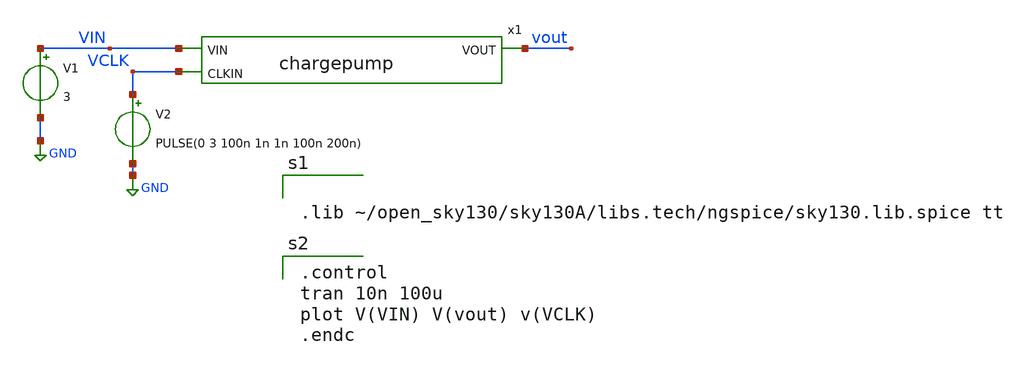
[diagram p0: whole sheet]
** sch_path: xschem/charge_pump/chargepump_tb.sch
**.subckt chargepump_tb
x1 VIN vout VCLK chargepump
V1 VIN GND 3
V2 VCLK GND PULSE(0 3 100n 1n 1n 100n 200n)
**** begin user architecture code


.lib ~/open_sky130/sky130A/libs.tech/ngspice/sky130.lib.spice tt


.control
tran 10n 100u
plot V(VIN) V(vout) v(VCLK)
.endc

**** end user architecture code
**.ends

* expanding   symbol:  chargepump.sym # of pins=3
** sym_path: xschem/charge_pump/chargepump.sym
** sch_path: xschem/charge_pump/chargepump.sch
.subckt chargepump VIN VOUT CLKIN
*.ipin VIN
*.ipin CLKIN
*.opin VOUT
XM2 VOUT net1 net1 net1 sky130_fd_pr__nfet_03v3_nvt L=0.5 W=1 nf=1 ad='int((nf+1)/2) * W/nf * 0.29' as='int((nf+2)/2) * W/nf * 0.29'
+ pd='2*int((nf+1)/2) * (W/nf + 0.29)' ps='2*int((nf+2)/2) * (W/nf + 0.29)' nrd='0.29 / W' nrs='0.29 / W'
+ sa=0 sb=0 sd=0 mult=1 m=1
XM1 VOUT net1 net1 net1 sky130_fd_pr__nfet_03v3_nvt L=0.5 W=1 nf=1 ad='int((nf+1)/2) * W/nf * 0.29' as='int((nf+2)/2) * W/nf * 0.29'
+ pd='2*int((nf+1)/2) * (W/nf + 0.29)' ps='2*int((nf+2)/2) * (W/nf + 0.29)' nrd='0.29 / W' nrs='0.29 / W'
+ sa=0 sb=0 sd=0 mult=1 m=1
XM3 net1 VIN VIN VIN sky130_fd_pr__nfet_03v3_nvt L=0.5 W=1 nf=1 ad='int((nf+1)/2) * W/nf * 0.29' as='int((nf+2)/2) * W/nf * 0.29'
+ pd='2*int((nf+1)/2) * (W/nf + 0.29)' ps='2*int((nf+2)/2) * (W/nf + 0.29)' nrd='0.29 / W' nrs='0.29 / W'
+ sa=0 sb=0 sd=0 mult=1 m=1
XM4 net1 VIN VIN VIN sky130_fd_pr__nfet_03v3_nvt L=0.5 W=1 nf=1 ad='int((nf+1)/2) * W/nf * 0.29' as='int((nf+2)/2) * W/nf * 0.29'
+ pd='2*int((nf+1)/2) * (W/nf + 0.29)' ps='2*int((nf+2)/2) * (W/nf + 0.29)' nrd='0.29 / W' nrs='0.29 / W'
+ sa=0 sb=0 sd=0 mult=1 m=1
XC1 net1 CLKIN sky130_fd_pr__cap_mim_m3_1 W=3e+07u L=3e+07u MF=100 m=100
XC2 VOUT GND sky130_fd_pr__cap_mim_m3_1 W=3e+07u L=3e+07u MF=100 m=100
.ends

.GLOBAL GND
.end
